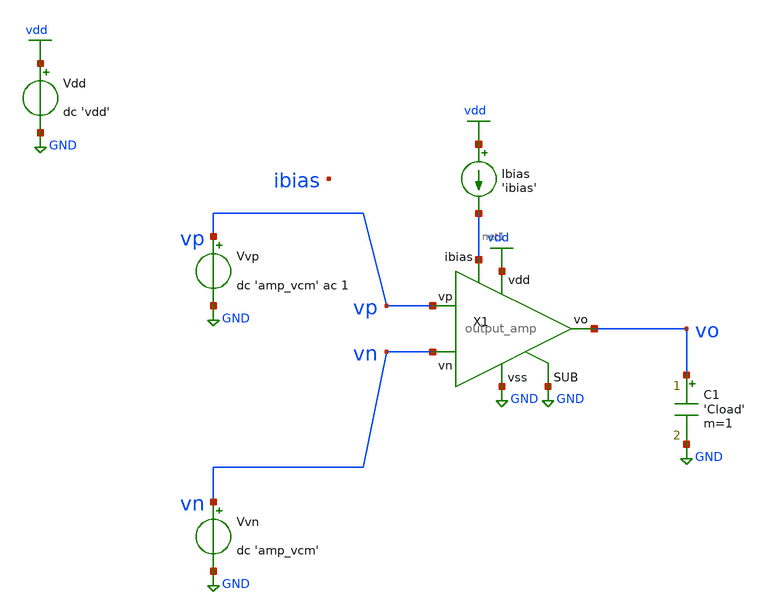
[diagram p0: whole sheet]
** sch_path: tb/output_amp/tb_amp_openloop_ac.sch
**.subckt tb_amp_openloop_ac
X1 vdd vo vp vn net1 GND GND output_amp
Vdd vdd GND dc 'vdd'
Vvp vp GND dc 'amp_vcm' ac 1
Vvn vn GND dc 'amp_vcm'
Ibias vdd net1 'ibias'
C1 vo GND 'Cload' m=1
**** begin user architecture code


.lib 'models_dir'/cornerMOShv.lib 'mos_corner'
.lib 'models_dir'/cornerCAP.lib cap_typ
.option TEMP='temperature'
.option warn=1
.control
save all
ac dec 20 10 100Meg
set wr_singlescale
wrdata 'simpath'/'filename'_'N'.data vdb(vo) vp(vo)
quit
.endc


**** end user architecture code
**.ends
.GLOBAL GND
.GLOBAL vdd
.end
